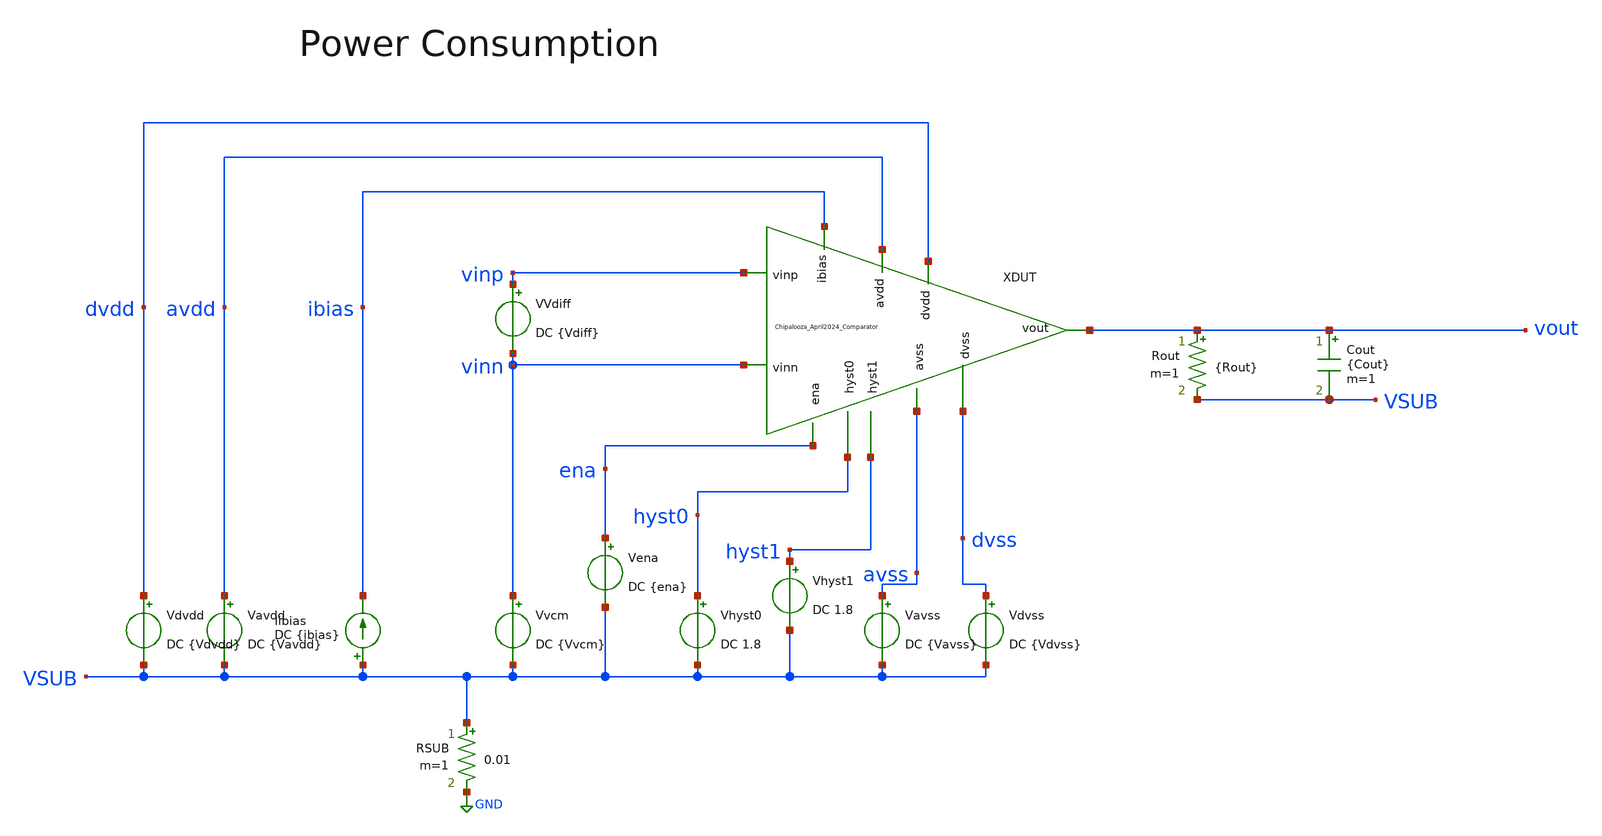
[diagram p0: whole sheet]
** sch_path: Chipalooza_April2024_Comparator/cace/powerConsumption.sch
**.subckt powerConsumption
Vavdd avdd VSUB DC {Vavdd}
Rout vout VSUB {Rout} m=1
Cout vout VSUB {Cout} m=1
Vdvdd dvdd VSUB DC {Vdvdd}
Vvcm vinn VSUB DC {Vvcm}
Vena ena VSUB DC {ena}
Vhyst0 hyst0 VSUB DC 1.8
Vavss avss VSUB DC {Vavss}
Vdvss dvss VSUB DC {Vdvss}
RSUB VSUB GND 0.01 m=1
Iibias VSUB ibias DC {ibias}
VVdiff vinp vinn DC {Vdiff}
XDUT hyst0 hyst1 avdd vinp avss vinn dvdd dvss vout ibias ena Chipalooza_April2024_Comparator
Vhyst1 hyst1 VSUB DC 1.8
**** begin user architecture code

.control
op

set wr_singlescale
wrdata {simpath}/{filename}_{N}.data -I(Vdvdd)
write ngspice/powerConsumption.raw

quit

.endc



* CACE gensim simulation file {filename}_{N}
* Generated by CACE gensim, Efabless Corporation (c) 2023
* Find the current through the amplifier under condition of static input

.include {DUT_path}

.lib {PDK_ROOT}/{PDK}/libs.tech/combined/sky130.lib.spice {corner}

.option TEMP={temperature}
* Flag unsafe operating conditions (exceeds models' specified limits)
.option warn=1
.option savecurrents
.option save all


**** end user architecture code
**.ends
.GLOBAL GND
.end
